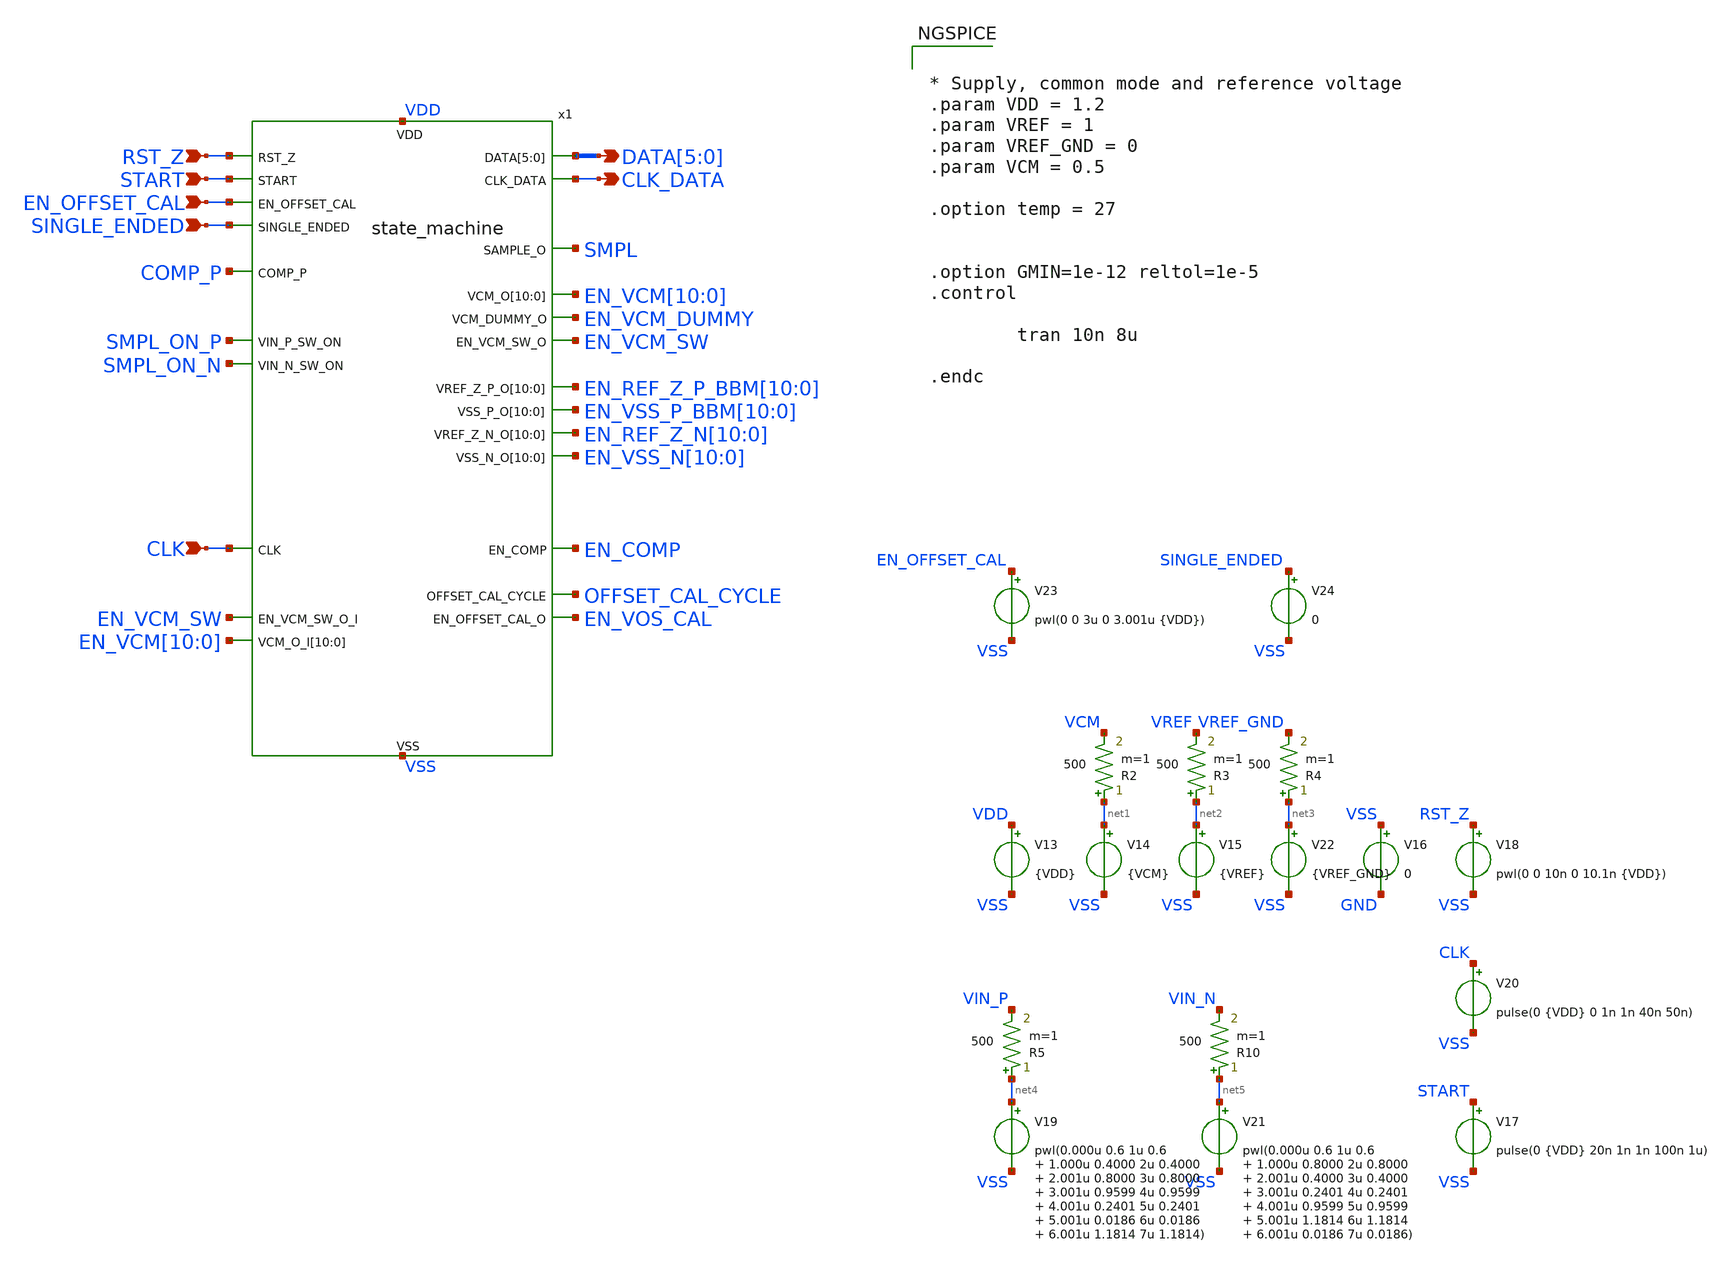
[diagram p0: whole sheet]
** sch_path: schematic/state_machine/state_machine_test.sch


* Models for standard digital cells
.include $PDK_ROOT/ihp-sg13g2/libs.ref/sg13g2_stdcell/spice/sg13g2_stdcell.spice

* Spice netlist for state machine generated by openlane
.include $HOME/schematic/state_machine/state_machine.spice

**.subckt state_machine_test RST_Z START CLK_DATA DATA[5],DATA[4],DATA[3],DATA[2],DATA[1],DATA[0]
*+ EN_OFFSET_CAL CLK SINGLE_ENDED
*.ipin RST_Z
*.ipin START
*.opin CLK_DATA
*.opin DATA[5],DATA[4],DATA[3],DATA[2],DATA[1],DATA[0]
*.ipin EN_OFFSET_CAL
*.ipin CLK
*.ipin SINGLE_ENDED
V13 VDD VSS {VDD}
.save i(v13)
V14 net1 VSS {VCM}
.save i(v14)
V15 net2 VSS {VREF}
.save i(v15)
V16 VSS GND 0
V17 START VSS pulse(0 {VDD} 20n 1n 1n 100n 1u)
V18 RST_Z VSS pwl(0 0 10n 0 10.1n {VDD})
V19 net4 VSS pwl(0.000u 0.6 1u 0.6 1.000u 0.4000 2u 0.4000 2.001u 0.8000 3u 0.8000 3.001u 0.9599 4u
+ 0.9599 4.001u 0.2401 5u 0.2401 5.001u 0.0186 6u 0.0186 6.001u 1.1814 7u 1.1814)
R2 net1 VCM 500 m=1
V20 CLK VSS pulse(0 {VDD} 0 1n 1n 40n 50n)
V21 net5 VSS pwl(0.000u 0.6 1u 0.6 1.000u 0.8000 2u 0.8000 2.001u 0.4000 3u 0.4000 3.001u 0.2401 4u
+ 0.2401 4.001u 0.9599 5u 0.9599 5.001u 1.1814 6u 1.1814 6.001u 0.0186 7u 0.0186)
V22 net3 VSS {VREF_GND}
.save i(v22)
R3 net2 VREF 500 m=1
R4 net3 VREF_GND 500 m=1
R5 net4 VIN_P 500 m=1
R10 net5 VIN_N 500 m=1
V23 EN_OFFSET_CAL VSS pwl(0 0 3u 0 3.001u {VDD})
V24 SINGLE_ENDED VSS 0
**** begin user architecture code


* Supply, common mode and reference voltage
.param VDD = 1.2
.param VREF = 1
.param VREF_GND = 0
.param VCM = 0.5

.option temp = 27


.option GMIN=1e-12 reltol=1e-5
.control

		tran 10n 8u

.endc


 .lib cornerMOSlv.lib mos_tt
.lib cornerMOShv.lib mos_tt
.lib $::SG13G2_MODELS/cornerRES.lib res_typ_stat


**** end user architecture code
**.ends
.end
